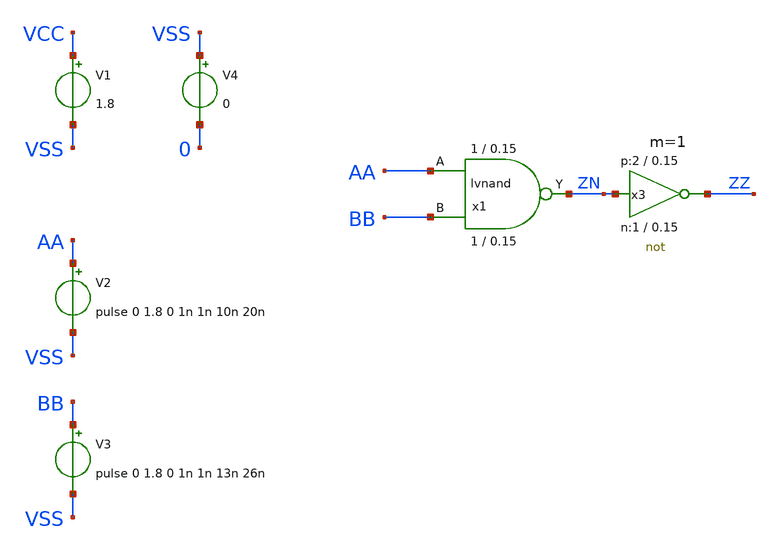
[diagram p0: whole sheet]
** sch_path: sky130_tests/logic_ngspice.sch
* Copyright 2020 Stefan Frederik Schippers
* Licensed under the Apache License, Version 2.0 (the "License");
* you may not use this file except in compliance with the License.
* You may obtain a copy of the License at
* https://www.apache.org/licenses/LICENSE-2.0
* Unless required by applicable law or agreed to in writing, software
* distributed under the License is distributed on an "AS IS" BASIS,
* WITHOUT WARRANTIES OR CONDITIONS OF ANY KIND, either express or implied.
* See the License for the specific language governing permissions and
* limitations under the License.
* sky130_tests/lvnand.sch:
* Copyright 2021 Stefan Frederik Schippers
**.subckt logic_ngspice
x1 AA BB ZN lvnand WidthN=1 LenN=0.15 WidthP=1 LenP=0.15 m=1
V1 VCC VSS 1.8
V2 AA VSS pulse 0 1.8 0 1n 1n 10n 20n
V3 BB VSS pulse 0 1.8 0 1n 1n 13n 26n
x3 ZZ ZN VCC VSS not W_N=1 L_N=0.15 W_P=2 L_P=0.15 m=1
V4 VSS 0 0
**** begin user architecture code


.control
tran 0.1n 200n
save all
plot aa bb+2 zz+4
.endc


 ** manual skywater pdks install (with patches applied)
* .lib $::SKYWATER_MODELS/models/sky130.lib.spice tt

** opencircuitdesign pdks install
.lib $::SKYWATER_MODELS/sky130.lib.spice tt

.param mc_mm_switch=0
.param mc_pr_switch=0

**** end user architecture code
**.ends

* expanding   symbol:  sky130_tests/lvnand.sym # of pins=3
** sym_path: sky130_tests/lvnand.sym
** sch_path: sky130_tests/lvnand.sch
.subckt lvnand A B Y  WidthN=1 LenN=0.15 WidthP=1 LenP=0.15
*.ipin A
*.ipin B
*.opin Y
XM1 Y B S VSSPIN sky130_fd_pr__nfet_01v8 L=LenN W=WidthN nf=1 ad='int((nf+1)/2) * W/nf * 0.29' as='int((nf+2)/2) * W/nf * 0.29'
+ pd='2*int((nf+1)/2) * (W/nf + 0.29)' ps='2*int((nf+2)/2) * (W/nf + 0.29)' nrd='0.29 / W' nrs='0.29 / W'
+ sa=0 sb=0 sd=0 mult=1 m=1
XM2 Y A VCCPIN VCCPIN sky130_fd_pr__pfet_01v8 L=LenP W=WidthP nf=1 ad='int((nf+1)/2) * W/nf * 0.29' as='int((nf+2)/2) * W/nf * 0.29'
+ pd='2*int((nf+1)/2) * (W/nf + 0.29)' ps='2*int((nf+2)/2) * (W/nf + 0.29)' nrd='0.29 / W' nrs='0.29 / W'
+ sa=0 sb=0 sd=0 mult=1 m=1
XM3 Y B VCCPIN VCCPIN sky130_fd_pr__pfet_01v8 L=LenP W=WidthP nf=1 ad='int((nf+1)/2) * W/nf * 0.29' as='int((nf+2)/2) * W/nf * 0.29'
+ pd='2*int((nf+1)/2) * (W/nf + 0.29)' ps='2*int((nf+2)/2) * (W/nf + 0.29)' nrd='0.29 / W' nrs='0.29 / W'
+ sa=0 sb=0 sd=0 mult=1 m=1
XM4 S A VSSPIN VSSPIN sky130_fd_pr__nfet_01v8 L=LenN W=WidthN nf=1 ad='int((nf+1)/2) * W/nf * 0.29' as='int((nf+2)/2) * W/nf * 0.29'
+ pd='2*int((nf+1)/2) * (W/nf + 0.29)' ps='2*int((nf+2)/2) * (W/nf + 0.29)' nrd='0.29 / W' nrs='0.29 / W'
+ sa=0 sb=0 sd=0 mult=1 m=1
.ends


* expanding   symbol:  sky130_tests/not.sym # of pins=2
** sym_path: sky130_tests/not.sym
** sch_path: sky130_tests/not.sch
.subckt not y a VCCPIN VSSPIN     W_N=1 L_N=0.15 W_P=2 L_P=0.15
*.opin y
*.ipin a
XM1 DN a VSSPIN VSSPIN sky130_fd_pr__nfet_01v8 L=L_N W=W_N nf=1 ad='int((1 + 1)/2) * W_N / 1 * 0.29'
+ as='int((1 + 2)/2) * W_N / 1 * 0.29' pd='2*int((1 + 1)/2) * (W_N / 1 + 0.29)' ps='2*int((1 + 2)/2) * (W_N / 1 + 0.29)'
+ nrd='0.29 / W_N ' nrs='0.29 / W_N ' sa=0 sb=0 sd=0 mult=1 m=1
XM2 DP a VCCPIN VCCPIN sky130_fd_pr__pfet_01v8 L=L_P W=W_P nf=1 ad='int((nf+1)/2) * W/nf * 0.29' as='int((nf+2)/2) * W/nf * 0.29'
+ pd='2*int((nf+1)/2) * (W/nf + 0.29)' ps='2*int((nf+2)/2) * (W/nf + 0.29)' nrd='0.29 / W' nrs='0.29 / W'
+ sa=0 sb=0 sd=0 mult=1 m=1
Vmeas DP y 0
.save i(vmeas)
Vmeas1 y DN 0
.save i(vmeas1)
.save v(dp)
.save v(dn)
.ends

.end
